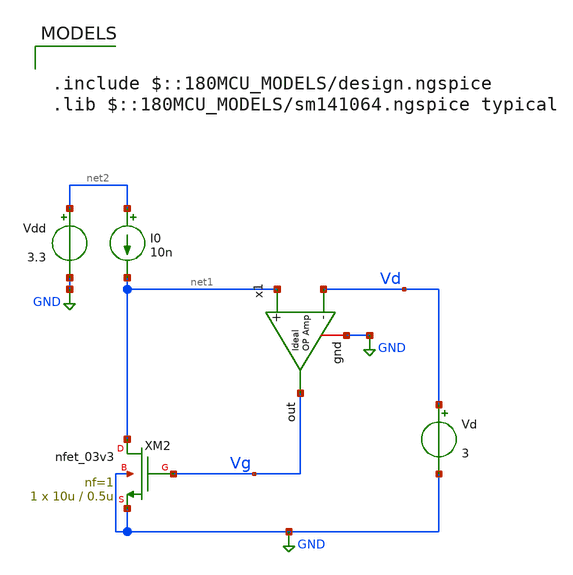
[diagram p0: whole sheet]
** sch_path: Examples/GF180MCU/xschem/Extraction/nmos_sigma_ext.sch
**.subckt nmos_sigma_ext
x1 Vg net1 Vd GND ampOp_ideal
XM2 net1 Vg GND GND nfet_03v3 L=0.5u W=10u nf=1 ad='int((nf+1)/2) * W/nf * 0.18u' as='int((nf+2)/2) * W/nf * 0.18u'
+ pd='2*int((nf+1)/2) * (W/nf + 0.18u)' ps='2*int((nf+2)/2) * (W/nf + 0.18u)' nrd='0.18u / W' nrs='0.18u / W'
+ sa=0 sb=0 sd=0 m=1
I0 net2 net1 10n
Vd Vd GND 3
Vdd net2 GND 3.3
**** begin user architecture code

.include $::180MCU_MODELS/design.ngspice
.lib $::180MCU_MODELS/sm141064.ngspice typical




.control
save all

dc Vd 0.2 3.5 25.9m

let vd_interp = 3.3/3
let sigma = -deriv(V(vg))/deriv(V(vd))
save sigma

echo
echo
echo


echo Sigma @ VD=$&vd_interp:
meas dc sigma_value FIND sigma WHEN V(vd)=vd_interp

echo
echo
echo
write nmos_sigma_ext.raw

.endc




**** end user architecture code
**.ends

* expanding   symbol:  /home/gmaranhao/Desktop/gf180_work/auxLib/ampOp_ideal.sym # of pins=4
** sym_path: /home/gmaranhao/Desktop/gf180_work/auxLib/ampOp_ideal.sym
** sch_path: /home/gmaranhao/Desktop/gf180_work/auxLib/ampOp_ideal.sch
.subckt ampOp_ideal out + - gnd
*.ipin +
*.ipin -
*.opin out
*.iopin gnd
E1 out gnd + - 10000000
.ends

.GLOBAL GND
.end
